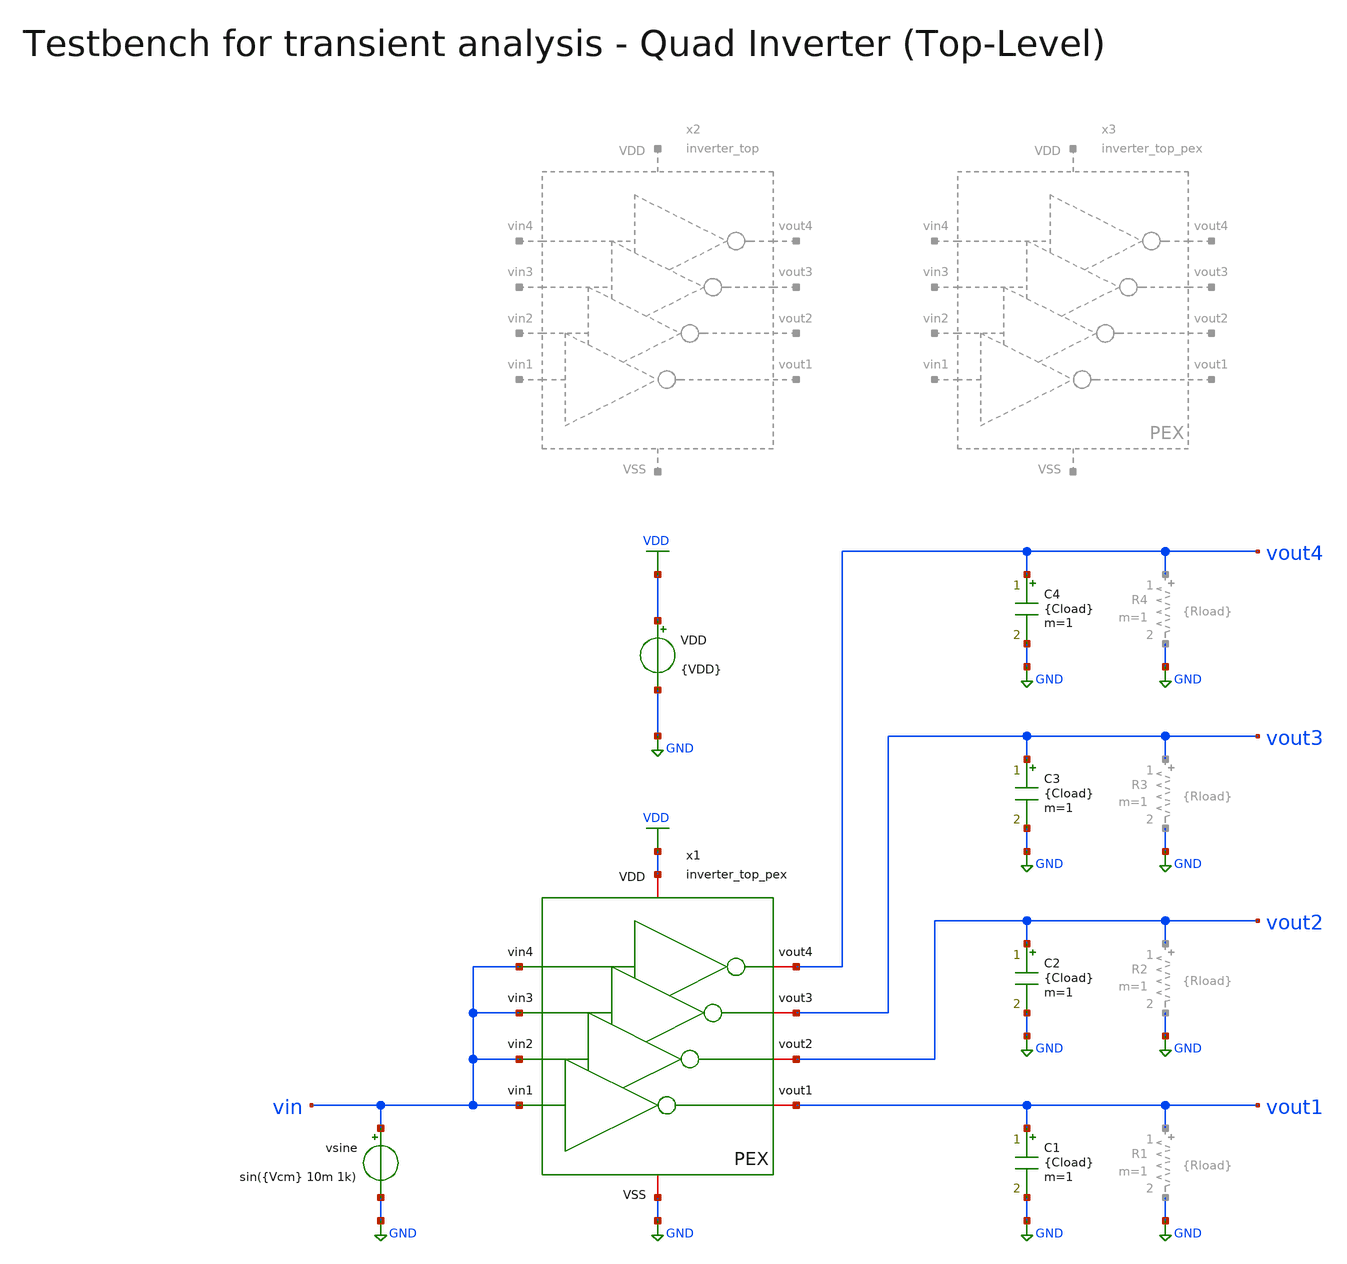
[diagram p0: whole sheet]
** sch_path: macros/inverter/testbenches/inverter_top_tb_tran.sch
**.subckt inverter_top_tb_tran
VDD VDD GND {VDD}
vsine vin GND sin({Vcm} 10m 1k)
C1 vout1 GND {Cload} m=1
C2 vout2 GND {Cload} m=1
C3 vout3 GND {Cload} m=1
C4 vout4 GND {Cload} m=1
x1 VDD vin vout4 GND vin vout3 vin vout2 vout1 vin inverter_top_pex
**** begin user architecture code


.include ../../netlist/pex/inverter_top_magic_pex_3.spice
.param VDD=1.5
.csparam VDD=VDD
.param Vcm=VDD/2
.param temp=27
.param Cload=10p
.param Rload=1k
.options savecurrents klu method=gear reltol=1e-4 abstol=1e-15 gmin=1e-15
.control

* save vin vinp vinn voutp voutn vout
save all

* Operating Point Analysis
op
remzerovec
write @schname\.raw
set appendwrite

* Transient Analysis
* Sine Input
tran 1u 5m
* Pulse Input
* tran 500n 1m
write @schname\.raw

* Plotting
plot vin vout1 vout2 vout3 vout4
* plot i(VDD)

* Measurements
meas tran vin_peak MAX v(vin)
meas tran vout_peak MAX v(vout1)

let Adm = vout_peak / vin_peak
let Adm_dB = vdb(Adm)
print Adm_dB

meas tran vout_pp_max MAX v(vout1)
meas tran vout_pp_min MIN v(vout1)
let vout_pp = vout_pp_max - vout_pp_min
print vout_pp

* Write Data
unset appendwrite
set wr_vecnames
set wr_singlescale
wrdata ../../scripts/plot_simulations/data/@schname\.txt  v(vin) v(vout1) v(vout2) v(vout3) v(vout4)

*quit
.endc



.lib cornerMOSlv.lib mos_tt
.lib cornerMOShv.lib mos_tt
.lib cornerHBT.lib hbt_typ
.lib cornerRES.lib res_typ
.lib cornerCAP.lib cap_typ
.lib cornerDIO.lib dio_tt

**** end user architecture code
**.ends
.GLOBAL GND
.GLOBAL VDD
.end
